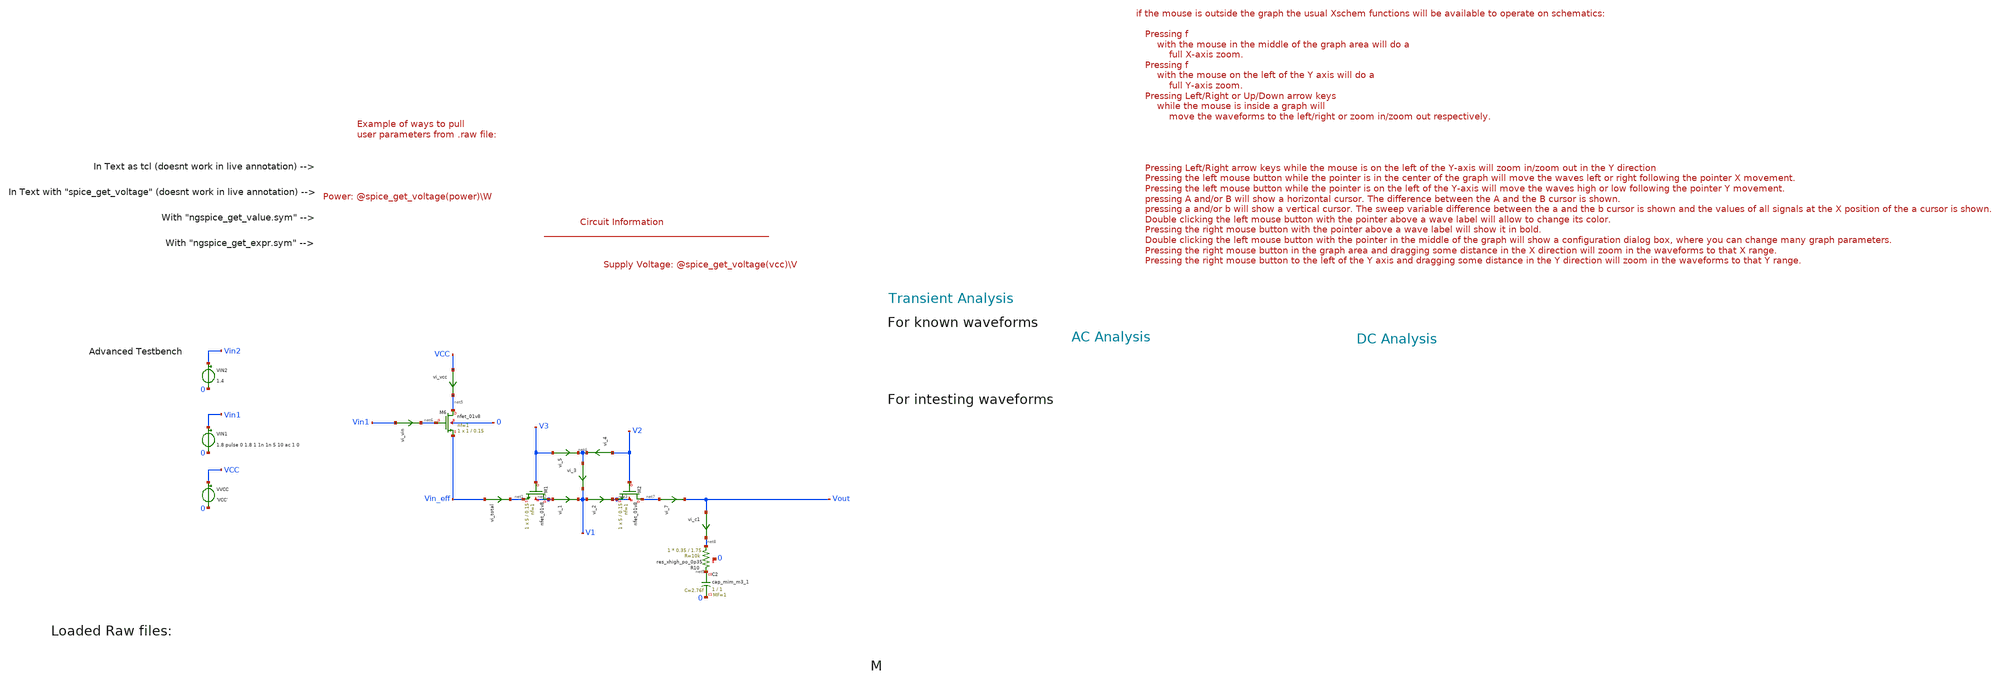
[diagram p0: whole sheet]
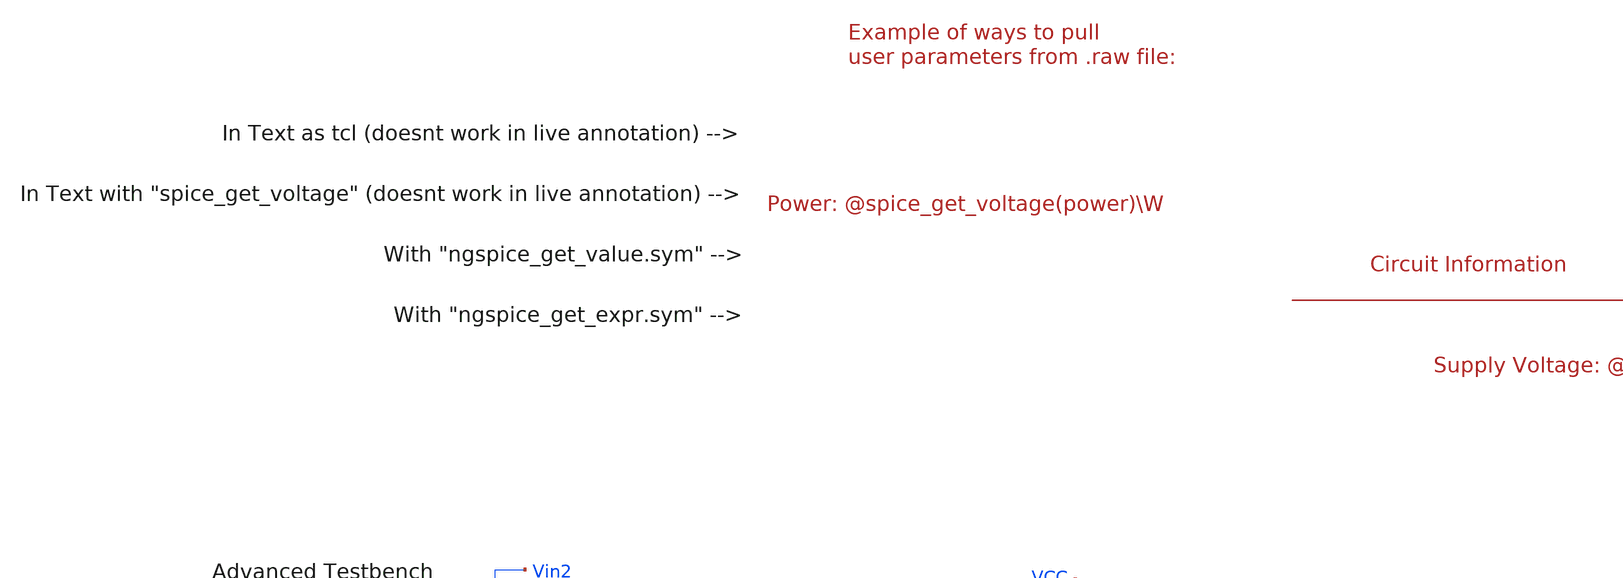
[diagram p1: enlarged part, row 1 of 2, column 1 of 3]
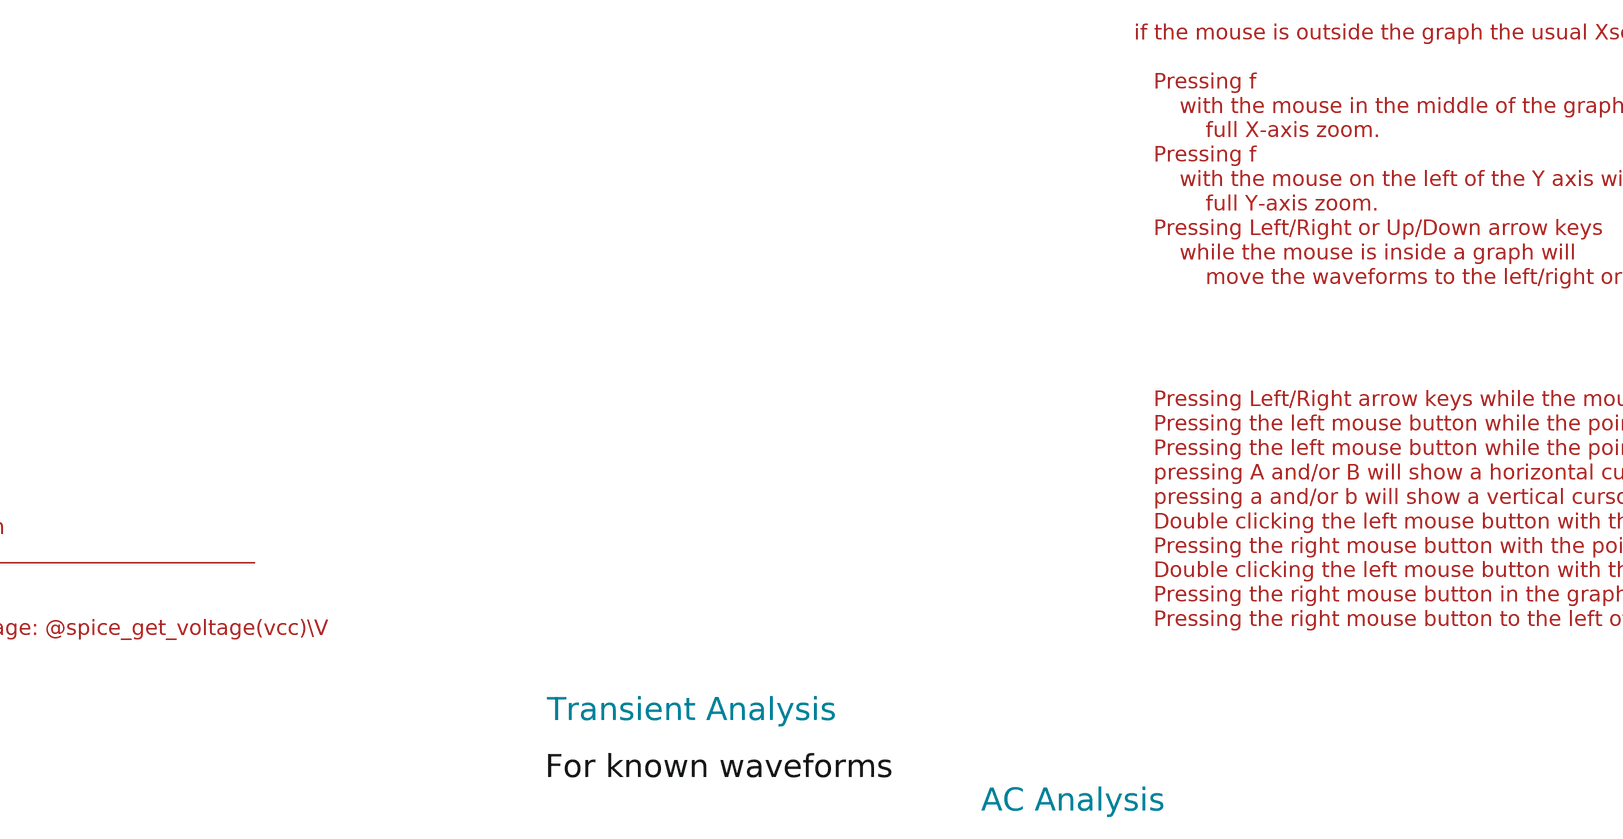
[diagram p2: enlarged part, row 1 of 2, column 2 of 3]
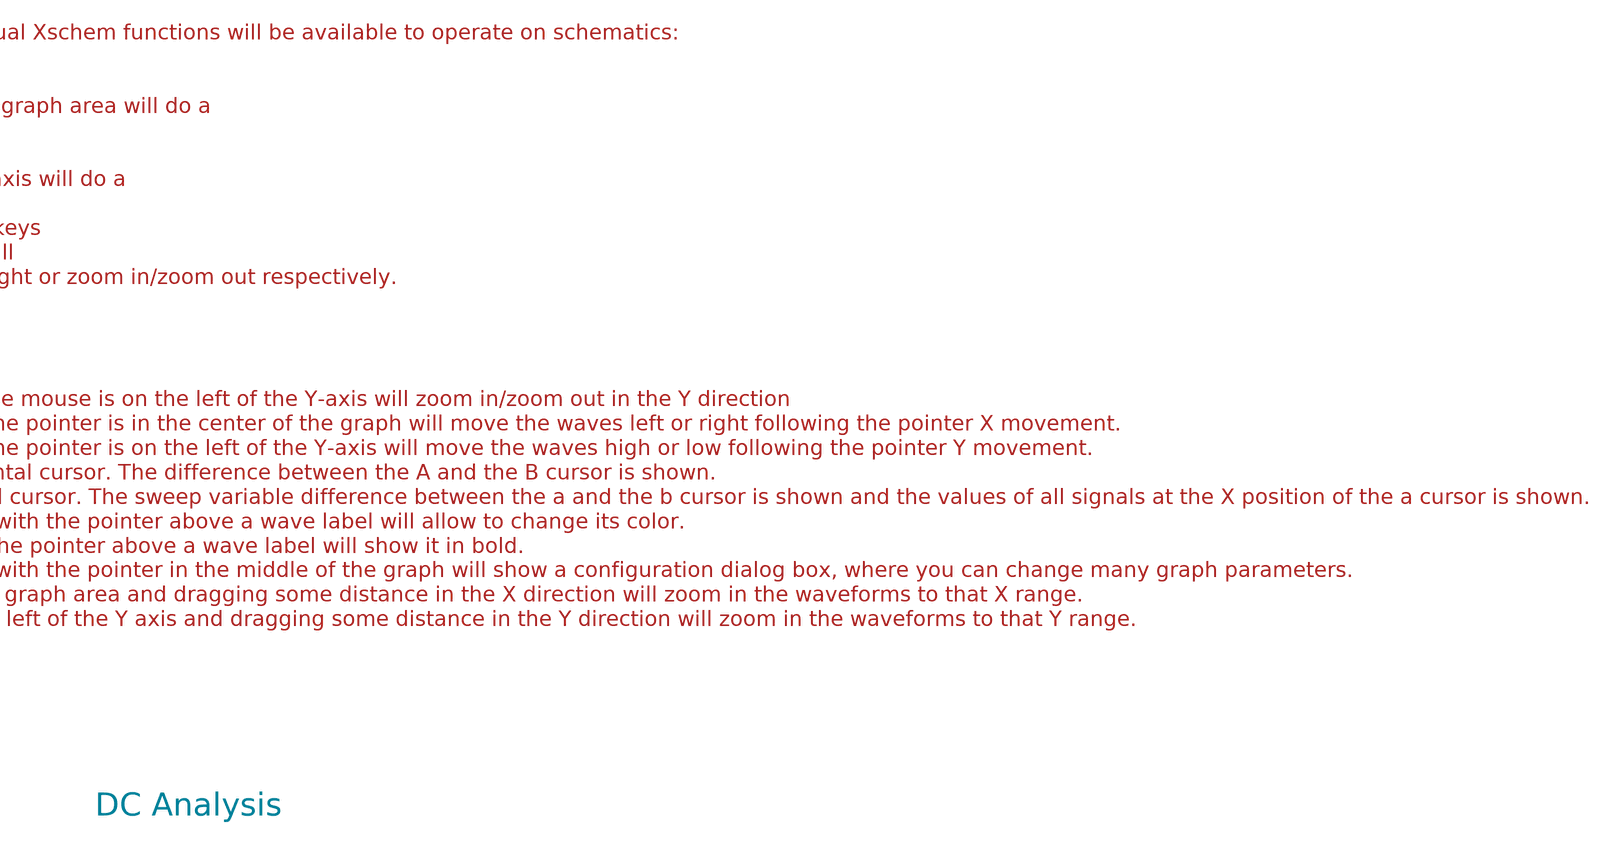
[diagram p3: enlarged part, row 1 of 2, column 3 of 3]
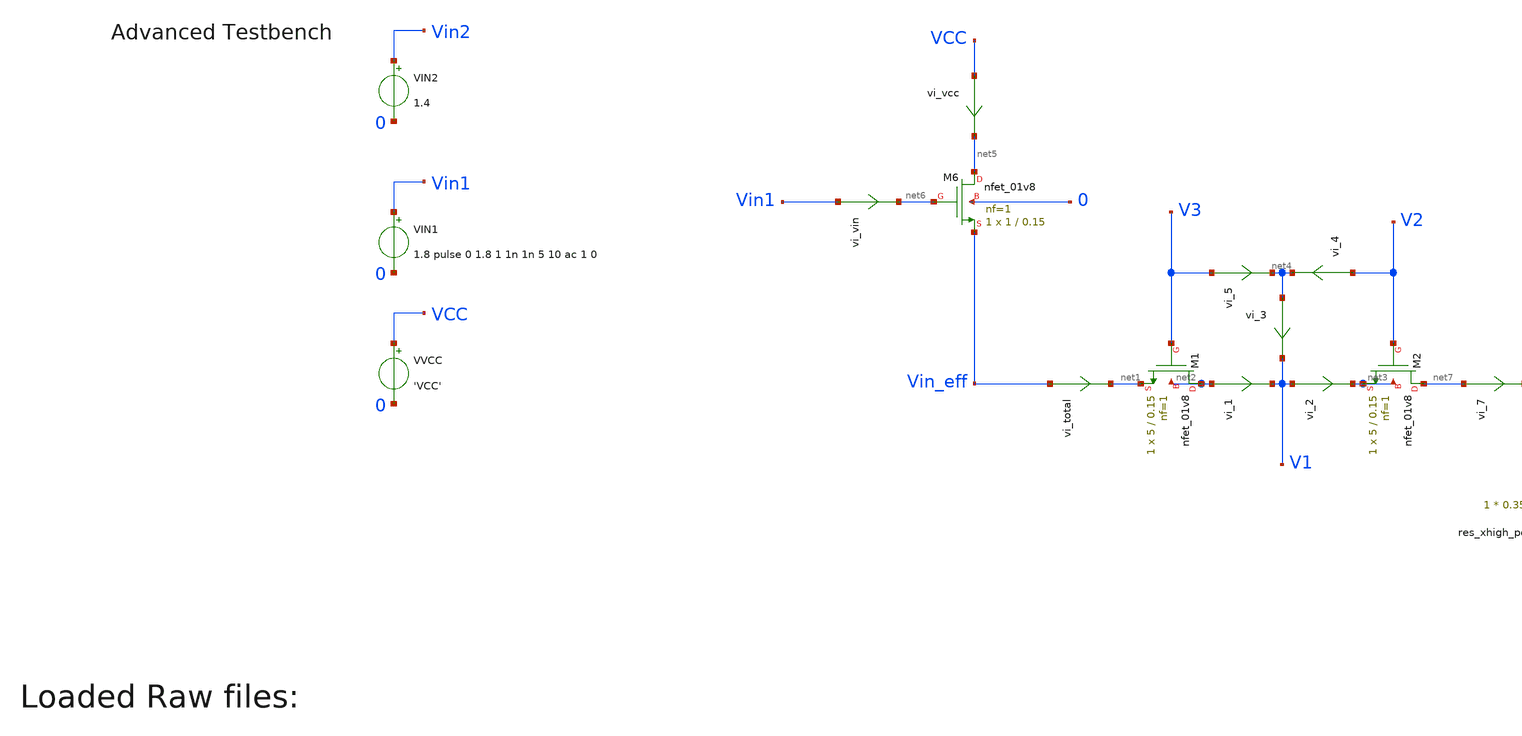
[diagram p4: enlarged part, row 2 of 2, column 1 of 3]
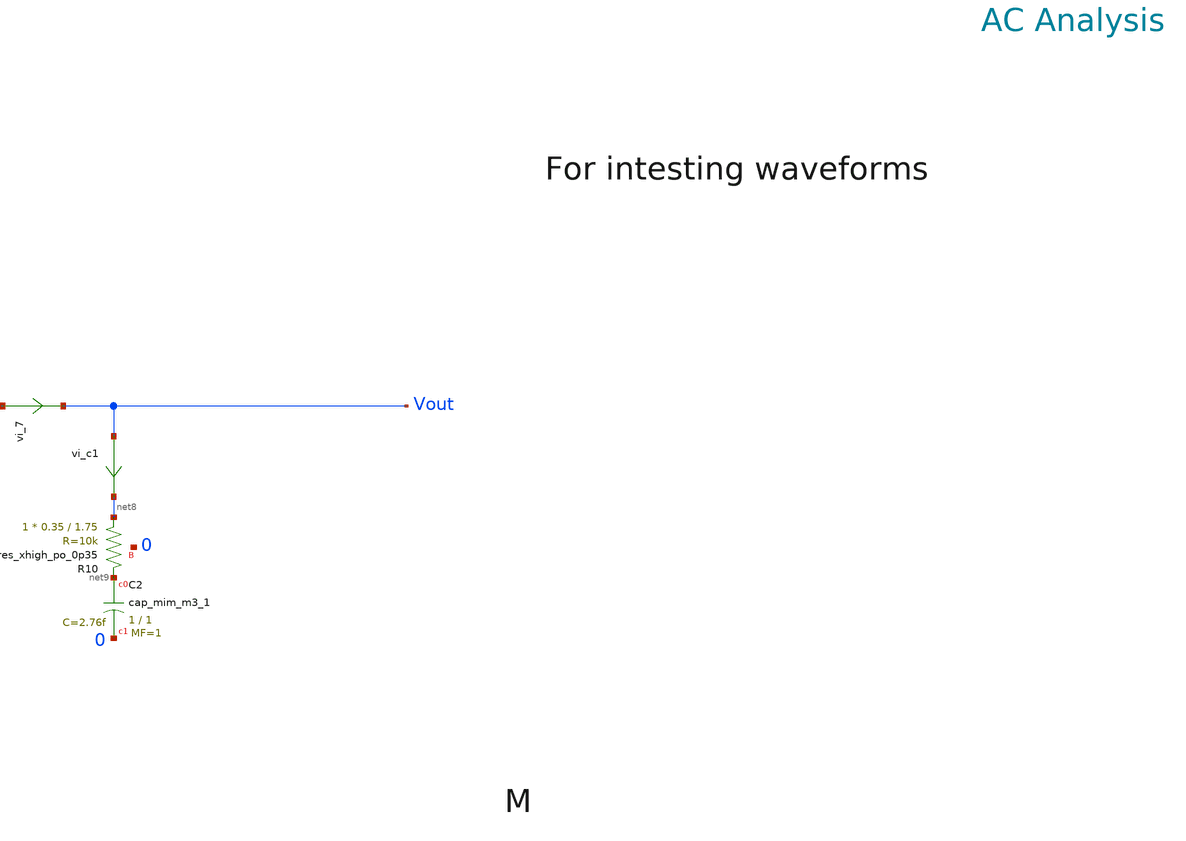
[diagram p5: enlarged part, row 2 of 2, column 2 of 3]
** sch_path: tt10-hdl/tt_um_test_commit/xschem/T0/mosRes/mosRes_tb.sch
* Copyright (C) 1998-2024 Stefan Frederik Schippers
* This program is free software; you can redistribute it and/or modify
* it under the terms of the GNU General Public License as published by
* the Free Software Foundation; either version 2 of the License, or
* (at your option) any later version.
* This program is distributed in the hope that it will be useful,
* but WITHOUT ANY WARRANTY; without even the implied warranty of
* MERCHANTABILITY or FITNESS FOR A PARTICULAR PURPOSE.  See the
* GNU General Public License for more details.
* You should have received a copy of the GNU General Public License
* along with this program; if not, write to the Free Software
**.subckt mosRes_tb
VVCC VCC 0 'VCC'
VIN1 Vin1 0 1.8 pulse 0 1.8 1 1n 1n 5 10 ac 1 0
VIN2 Vin2 0 1.4
vi_total Vin_eff net1 0
.save i(vi_total)
XM1 net2 V3 net1 net2 sky130_fd_pr__nfet_01v8 L=0.15 W=5 nf=1 ad='int((1 + 1)/2) * 5 / 1 * 0.29' as='int((1 + 2)/2) * 5 / 1 * 0.29'
+ pd='2*int((1 + 1)/2) * (5 / 1 + 0.29)' ps='2*int((1 + 2)/2) * (5 / 1 + 0.29)' nrd='0.29 / 5 ' nrs='0.29 / 5 '
+ sa=0 sb=0 sd=0 mult=1 m=1
XM2 net7 V2 net3 net3 sky130_fd_pr__nfet_01v8 L=0.15 W=5 nf=1 ad='int((1 + 1)/2) * 5 / 1 * 0.29' as='int((1 + 2)/2) * 5 / 1 * 0.29'
+ pd='2*int((1 + 1)/2) * (5 / 1 + 0.29)' ps='2*int((1 + 2)/2) * (5 / 1 + 0.29)' nrd='0.29 / 5 ' nrs='0.29 / 5 '
+ sa=0 sb=0 sd=0 mult=1 m=1
vi_1 net2 V1 0
.save i(vi_1)
vi_2 V1 net3 0
.save i(vi_2)
vi_3 net4 V1 0
.save i(vi_3)
vi_5 V3 net4 0
.save i(vi_5)
vi_4 V2 net4 0
.save i(vi_4)
XM6 net5 net6 Vin_eff 0 sky130_fd_pr__nfet_01v8 L=0.15 W=1 nf=1 ad='int((1 + 1)/2) * 1 / 1 * 0.29' as='int((1 + 2)/2) * 1 / 1 * 0.29'
+ pd='2*int((1 + 1)/2) * (1 / 1 + 0.29)' ps='2*int((1 + 2)/2) * (1 / 1 + 0.29)' nrd='0.29 / 1 ' nrs='0.29 / 1 '
+ sa=0 sb=0 sd=0 mult=1 m=1
vi_vin Vin1 net6 0
.save i(vi_vin)
vi_vcc VCC net5 0
.save i(vi_vcc)
vi_7 net7 Vout 0
.save i(vi_7)
XC2 net9 0 sky130_fd_pr__cap_mim_m3_1 W=1 L=1 MF=1 m=1
vi_c1 Vout net8 0
.save i(vi_c1)
XR10 net8 net9 0 sky130_fd_pr__res_xhigh_po_0p35 L=1.75 mult=1 m=1
**** begin user architecture code



.temp 30
*.param IB=1n
.param VCC = 1.8

.option savecurrents
.save all @m1[gm] @m2[gm] @m3[gm]
.control
  save all alli
  op
  let power=-v(vcc) * i(vvcc)
  settype power power
  write template_adv_tb.raw
  set appendwrite

  *dc vin1 0 1.8 0.001
  *write template_adv_tb.raw

  *tran 10p 3n
  tran 1m 5
  write template_adv_tb.raw

  *ac dec 10 1 1G
  *remzerovec
  *write template_adv_tb.raw



  quit 0




.endc





** opencircuitdesign pdks install
.lib $::SKYWATER_MODELS/sky130.lib.spice tt


**** end user architecture code
**.ends
.end
